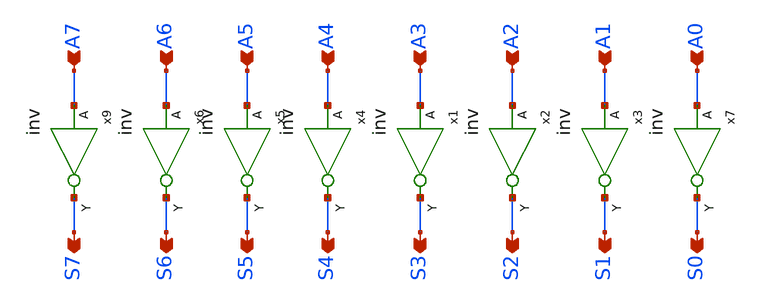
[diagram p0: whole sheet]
** sch_path: design/xschem/NOT/not8.sch
**.subckt not8 A7 A5 A6 A4 A3 A2 A1 A0 S7 S6 S5 S4 S3 S2 S1 S0
*.ipin A7
*.ipin A5
*.ipin A6
*.ipin A4
*.ipin A3
*.ipin A2
*.ipin A1
*.ipin A0
*.opin S7
*.opin S6
*.opin S5
*.opin S4
*.opin S3
*.opin S2
*.opin S1
*.opin S0
x1 A3 VSS VDD S3 inv
x2 A2 VSS VDD S2 inv
x3 A1 VSS VDD S1 inv
x4 A4 VSS VDD S4 inv
x5 A5 VSS VDD S5 inv
x6 A6 VSS VDD S6 inv
x7 A0 VSS VDD S0 inv
x9 A7 VSS VDD S7 inv
**.ends

* expanding   symbol:  INV/inv.sym # of pins=2
** sym_path: design/xschem/INV/inv.sym
** sch_path: design/xschem/INV/inv.sch
.subckt inv A VSS VDD Y
*.ipin A
*.opin Y
XM2 Y A VSS GND sky130_fd_pr__nfet_01v8 L=0.15 W=1 nf=1 ad='int((nf+1)/2) * W/nf * 0.29' as='int((nf+2)/2) * W/nf * 0.29'
+ pd='2*int((nf+1)/2) * (W/nf + 0.29)' ps='2*int((nf+2)/2) * (W/nf + 0.29)' nrd='0.29 / W' nrs='0.29 / W'
+ sa=0 sb=0 sd=0 mult=1 m=1
XM1 Y A VDD VDD sky130_fd_pr__pfet_01v8 L=0.15 W=3.21 nf=1 ad='int((nf+1)/2) * W/nf * 0.29' as='int((nf+2)/2) * W/nf * 0.29'
+ pd='2*int((nf+1)/2) * (W/nf + 0.29)' ps='2*int((nf+2)/2) * (W/nf + 0.29)' nrd='0.29 / W' nrs='0.29 / W'
+ sa=0 sb=0 sd=0 mult=1 m=1
.ends

.end
